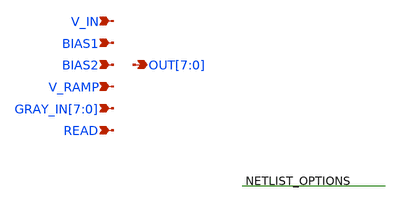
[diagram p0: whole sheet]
** sch_path: xschem/post_layout/adc_layout.sch
**.subckt adc_layout V_IN BIAS1 BIAS2 V_RAMP
*+ GRAY_IN[7],GRAY_IN[6],GRAY_IN[5],GRAY_IN[4],GRAY_IN[3],GRAY_IN[2],GRAY_IN[1],GRAY_IN[0] READ OUT[7],OUT[6],OUT[5],OUT[4],OUT[3],OUT[2],OUT[1],OUT[0]
*.ipin V_IN
*.ipin BIAS1
*.ipin BIAS2
*.ipin V_RAMP
*.ipin GRAY_IN[7],GRAY_IN[6],GRAY_IN[5],GRAY_IN[4],GRAY_IN[3],GRAY_IN[2],GRAY_IN[1],GRAY_IN[0]
*.ipin READ
*.opin OUT[7],OUT[6],OUT[5],OUT[4],OUT[3],OUT[2],OUT[1],OUT[0]
**.ends
**** begin user architecture code


X8bit_dram_0 READ GRAY_INx4x GRAY_INx2x OUTx6x GRAY_INx7x READ GRAY_INx0x OUTx4x OUTx2x  GRAY_INx5x
+ GRAY_INx3x OUTx7x OUTx0x GRAY_INx1x OUTx3x OUTx5x READ 8bit_dram_0/4bit_dram_1/dram_array_1/dram_cell_1/WWL
+  OUTx1x GRAY_INx6x GND x8bit_dram
X0 VDD a_1000_n1450# a_1000_n1450# VDD sky130_fd_pr__pfet_01v8_lvt ad=1.45e+12p pd=1.09e+07u
+ as=3.5e+11p ps=2.7e+06u w=1e+06u l=1e+06u
X1 8bit_dram_0/4bit_dram_1/dram_array_1/dram_cell_1/WWL a_1870_n1400# GND GND
+ sky130_fd_pr__nfet_01v8 ad=4e+11p pd=2.8e+06u as=2.5e+07p ps=5000u w=1e+06u l=150000u
X2 a_1720_n1450# V_RAMP a_1100_n1450# GND sky130_fd_pr__nfet_01v8_lvt ad=3.5e+11p pd=2.7e+06u
+ as=8.8e+11p ps=7.1e+06u w=1e+06u l=150000u
X3 a_1870_n1400# a_1720_n1450# VDD VDD sky130_fd_pr__pfet_01v8_lvt ad=3.5e+11p pd=2.7e+06u as=0p
+ ps=0u w=1e+06u l=450000u
X4 a_1100_n1450# V_IN a_1000_n1450# GND sky130_fd_pr__nfet_01v8_lvt ad=0p pd=0u as=3.5e+11p
+ ps=2.7e+06u w=1e+06u l=150000u
X5 8bit_dram_0/4bit_dram_1/dram_array_1/dram_cell_1/WWL a_1870_n1400# VDD VDD
+ sky130_fd_pr__pfet_01v8 ad=3.5e+11p pd=2.7e+06u as=0p ps=0u w=1e+06u l=200000u
X6 a_1100_n1450# BIAS1 GND GND sky130_fd_pr__nfet_01v8 ad=0p pd=0u as=0p ps=0u w=450000u l=1e+06u
X7 a_1870_n1400# BIAS2 GND GND sky130_fd_pr__nfet_01v8_lvt ad=3.5e+11p pd=2.7e+06u as=0p ps=0u
+ w=1e+06u l=1e+06u
X8 a_1720_n1450# a_1000_n1450# VDD VDD sky130_fd_pr__pfet_01v8_lvt ad=3.5e+11p pd=2.7e+06u as=0p
+ ps=0u w=1e+06u l=1e+06u

.subckt dram_cell storage WWL WBL RWL RBL VSUBS
X0 RWL storage RBL VSUBS sky130_fd_pr__nfet_01v8 ad=3e+11p pd=2.6e+06u as=3.5e+11p ps=2.7e+06u
+ w=1e+06u l=150000u
X1 storage WWL WBL VSUBS sky130_fd_pr__nfet_01v8 ad=3.5e+11p pd=2.7e+06u as=3e+11p ps=2.6e+06u
+ w=1e+06u l=150000u
.ends

.subckt dram_array dram_cell_1/WWL dram_cell_0/WBL dram_cell_1/RWL dram_cell_0/RBL  dram_cell_1/WBL
+ dram_cell_1/RBL VSUBS dram_cell_0/RWL
Xdram_cell_0 dram_cell_0/storage dram_cell_1/WWL dram_cell_0/WBL dram_cell_0/RWL dram_cell_0/RBL
+  VSUBS dram_cell
Xdram_cell_1 dram_cell_1/storage dram_cell_1/WWL dram_cell_1/WBL dram_cell_1/RWL dram_cell_1/RBL
+  VSUBS dram_cell
.ends

.subckt x4bit_dram dram_array_0/dram_cell_1/RBL dram_array_1/dram_cell_0/RWL
+ dram_array_1/dram_cell_1/WWL  dram_array_1/dram_cell_0/WBL dram_array_0/dram_cell_0/WBL dram_array_1/dram_cell_1/RWL
+  dram_array_1/dram_cell_0/RBL dram_array_1/dram_cell_1/WBL dram_array_0/dram_cell_0/RBL  dram_array_0/dram_cell_1/WBL
+ dram_array_1/dram_cell_1/RBL VSUBS
Xdram_array_0 dram_array_1/dram_cell_1/WWL dram_array_0/dram_cell_0/WBL dram_array_1/dram_cell_0/RWL
+  dram_array_0/dram_cell_0/RBL dram_array_0/dram_cell_1/WBL dram_array_0/dram_cell_1/RBL  VSUBS dram_array_1/dram_cell_0/RWL
+ dram_array
Xdram_array_1 dram_array_1/dram_cell_1/WWL dram_array_1/dram_cell_0/WBL dram_array_1/dram_cell_1/RWL
+  dram_array_1/dram_cell_0/RBL dram_array_1/dram_cell_1/WBL dram_array_1/dram_cell_1/RBL  VSUBS dram_array_1/dram_cell_0/RWL
+ dram_array
.ends

.subckt x8bit_dram 4bit_dram_1/dram_array_1/dram_cell_1/RWL 4bit_dram_1/dram_array_0/dram_cell_0/WBL
+  4bit_dram_0/dram_array_1/dram_cell_0/WBL 4bit_dram_1/dram_array_1/dram_cell_0/RBL  4bit_dram_1/dram_array_1/dram_cell_1/WBL
+ 4bit_dram_0/dram_array_1/dram_cell_1/RWL  4bit_dram_0/dram_array_0/dram_cell_0/WBL 4bit_dram_1/dram_array_0/dram_cell_0/RBL
+  4bit_dram_0/dram_array_1/dram_cell_0/RBL 4bit_dram_1/dram_array_0/dram_cell_1/WBL  4bit_dram_0/dram_array_1/dram_cell_1/WBL
+ 4bit_dram_1/dram_array_1/dram_cell_1/RBL  4bit_dram_0/dram_array_0/dram_cell_0/RBL 4bit_dram_0/dram_array_0/dram_cell_1/WBL
+  4bit_dram_0/dram_array_1/dram_cell_1/RBL 4bit_dram_1/dram_array_0/dram_cell_1/RBL  4bit_dram_1/dram_array_1/dram_cell_0/RWL
+ 4bit_dram_1/dram_array_1/dram_cell_1/WWL  4bit_dram_0/dram_array_0/dram_cell_1/RBL 4bit_dram_1/dram_array_1/dram_cell_0/WBL  VSUBS
X4bit_dram_1 4bit_dram_1/dram_array_0/dram_cell_1/RBL 4bit_dram_1/dram_array_1/dram_cell_0/RWL
+  4bit_dram_1/dram_array_1/dram_cell_1/WWL 4bit_dram_1/dram_array_1/dram_cell_0/WBL  4bit_dram_1/dram_array_0/dram_cell_0/WBL
+ 4bit_dram_1/dram_array_1/dram_cell_1/RWL  4bit_dram_1/dram_array_1/dram_cell_0/RBL 4bit_dram_1/dram_array_1/dram_cell_1/WBL
+  4bit_dram_1/dram_array_0/dram_cell_0/RBL 4bit_dram_1/dram_array_0/dram_cell_1/WBL  4bit_dram_1/dram_array_1/dram_cell_1/RBL VSUBS x4bit_dram
X4bit_dram_0 4bit_dram_0/dram_array_0/dram_cell_1/RBL 4bit_dram_1/dram_array_1/dram_cell_0/RWL
+  4bit_dram_1/dram_array_1/dram_cell_1/WWL 4bit_dram_0/dram_array_1/dram_cell_0/WBL  4bit_dram_0/dram_array_0/dram_cell_0/WBL
+ 4bit_dram_0/dram_array_1/dram_cell_1/RWL  4bit_dram_0/dram_array_1/dram_cell_0/RBL 4bit_dram_0/dram_array_1/dram_cell_1/WBL
+  4bit_dram_0/dram_array_0/dram_cell_0/RBL 4bit_dram_0/dram_array_0/dram_cell_1/WBL  4bit_dram_0/dram_array_1/dram_cell_1/RBL VSUBS x4bit_dram
.ends




**** end user architecture code
.end
